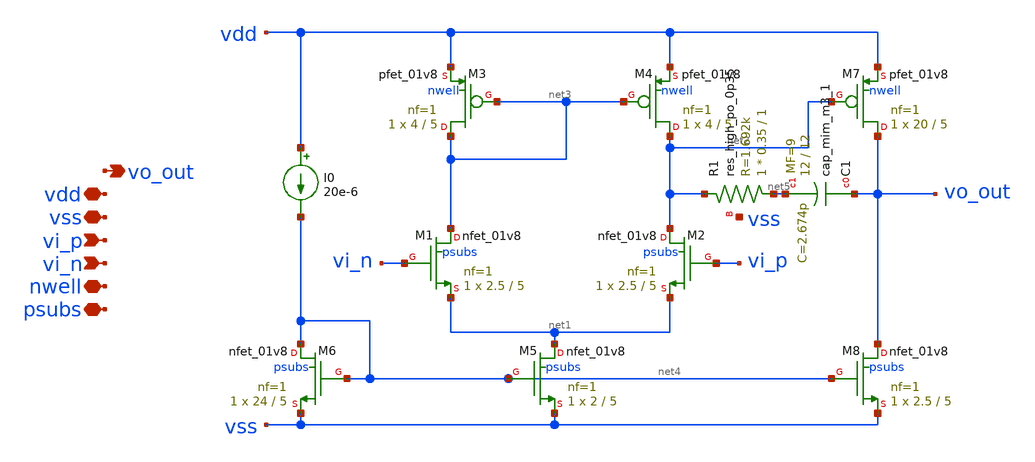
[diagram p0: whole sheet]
** sch_path: xschem/op.sch
**.subckt op vss vdd vo_out vi_p vi_n psubs nwell
*.iopin vss
*.iopin vdd
*.opin vo_out
*.ipin vi_p
*.ipin vi_n
*.iopin psubs
*.iopin nwell
XM1 net3 vi_n net1 psubs sky130_fd_pr__nfet_01v8 L=5 W=2.5 nf=1 ad='int((nf+1)/2) * W/nf * 0.29' as='int((nf+2)/2) * W/nf * 0.29'
+ pd='2*int((nf+1)/2) * (W/nf + 0.29)' ps='2*int((nf+2)/2) * (W/nf + 0.29)' nrd='0.29 / W' nrs='0.29 / W'
+ sa=0 sb=0 sd=0 mult=1 m=1
XM3 net3 net3 vdd nwell sky130_fd_pr__pfet_01v8 L=5 W=4 nf=1 ad='int((1 + 1)/2) * 4 / 1 * 0.29' as='int((1 + 2)/2) * 4 / 1 * 0.29'
+ pd='2*int((1 + 1)/2) * (4 / 1 + 0.29)' ps='2*int((1 + 2)/2) * (4 / 1 + 0.29)' nrd='0.29 / 4 ' nrs='0.29 / 4 '
+ sa=0 sb=0 sd=0 mult=1 m=1
XM6 net4 net4 vss psubs sky130_fd_pr__nfet_01v8 L=5 W=24 nf=1 ad='int((1 + 1)/2) * 24 / 1 * 0.29' as='int((1 + 2)/2) * 24 / 1 * 0.29'
+ pd='2*int((1 + 1)/2) * (24 / 1 + 0.29)' ps='2*int((1 + 2)/2) * (24 / 1 + 0.29)' nrd='0.29 / 24 ' nrs='0.29 / 24 '
+ sa=0 sb=0 sd=0 mult=1 m=1
I0 vdd net4 20e-6
XM5 net1 net4 vss psubs sky130_fd_pr__nfet_01v8 L=5 W=2 nf=1 ad='int((1 + 1)/2) * 2 / 1 * 0.29' as='int((1 + 2)/2) * 2 / 1 * 0.29'
+ pd='2*int((1 + 1)/2) * (2 / 1 + 0.29)' ps='2*int((1 + 2)/2) * (2 / 1 + 0.29)' nrd='0.29 / 2 ' nrs='0.29 / 2 '
+ sa=0 sb=0 sd=0 mult=1 m=1
XM7 vo_out net2 vdd nwell sky130_fd_pr__pfet_01v8 L=5 W=20 nf=1 ad='int((1 + 1)/2) * 20 / 1 * 0.29' as='int((1 + 2)/2) * 20 / 1 * 0.29'
+ pd='2*int((1 + 1)/2) * (20 / 1 + 0.29)' ps='2*int((1 + 2)/2) * (20 / 1 + 0.29)' nrd='0.29 / 20 ' nrs='0.29 / 20 '
+ sa=0 sb=0 sd=0 mult=1 m=1
XM8 vo_out net4 vss psubs sky130_fd_pr__nfet_01v8 L=5 W=2.5 nf=1 ad='int((1 + 1)/2) * 2.5 / 1 * 0.29'
+ as='int((1 + 2)/2) * 2.5 / 1 * 0.29' pd='2*int((1 + 1)/2) * (2.5 / 1 + 0.29)' ps='2*int((1 + 2)/2) * (2.5 / 1 + 0.29)'
+ nrd='0.29 / 2.5 ' nrs='0.29 / 2.5 ' sa=0 sb=0 sd=0 mult=1 m=1
XM2 net2 vi_p net1 psubs sky130_fd_pr__nfet_01v8 L=5 W=2.5 nf=1 ad='int((nf+1)/2) * W/nf * 0.29' as='int((nf+2)/2) * W/nf * 0.29'
+ pd='2*int((nf+1)/2) * (W/nf + 0.29)' ps='2*int((nf+2)/2) * (W/nf + 0.29)' nrd='0.29 / W' nrs='0.29 / W'
+ sa=0 sb=0 sd=0 mult=1 m=1
XM4 net2 net3 vdd nwell sky130_fd_pr__pfet_01v8 L=5 W=4 nf=1 ad='int((1 + 1)/2) * 4 / 1 * 0.29' as='int((1 + 2)/2) * 4 / 1 * 0.29'
+ pd='2*int((1 + 1)/2) * (4 / 1 + 0.29)' ps='2*int((1 + 2)/2) * (4 / 1 + 0.29)' nrd='0.29 / 4 ' nrs='0.29 / 4 '
+ sa=0 sb=0 sd=0 mult=1 m=1
XR1 net5 net2 vss sky130_fd_pr__res_high_po_0p35 L=1 mult=1 m=1
XC1 vo_out net5 sky130_fd_pr__cap_mim_m3_1 W=12 L=12 MF=9 m=9
**** begin user architecture code


.include ./sizing_opamp.spice


**** end user architecture code
**.ends
.end
